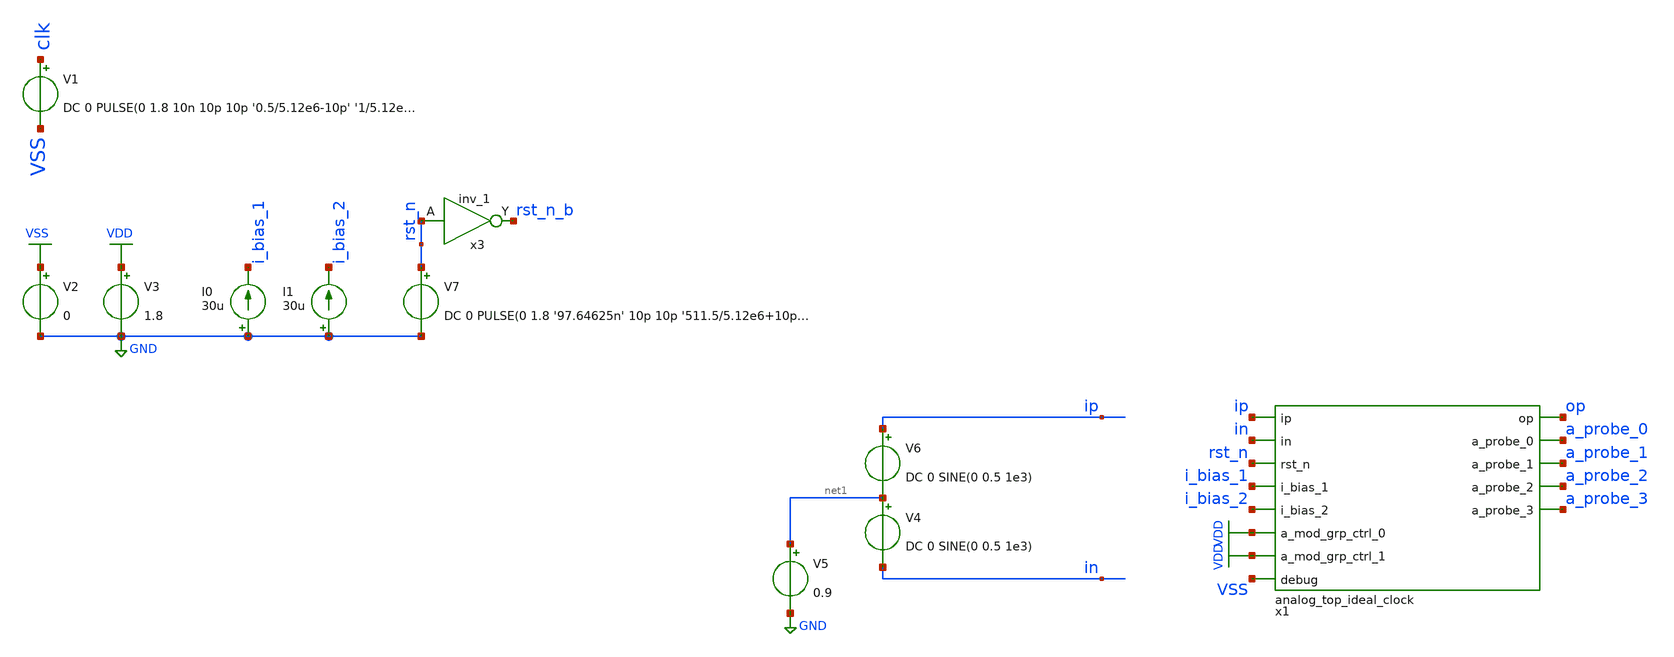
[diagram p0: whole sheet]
** sch_path: verification/schematic_sim/analog_top_ideal_clock_tb.sch
**.subckt analog_top_ideal_clock_tb
V1 clk VSS DC 0 PULSE(0 1.8 10n 10p 10p '0.5/5.12e6-10p' '1/5.12e6')
V2 VSS GND 0
V3 VDD GND 1.8
I0 GND i_bias_1 30u
I1 GND i_bias_2 30u
V5 net1 GND 0.9
V6 ip net1 DC 0 SINE(0 0.5 1e3)
V4 net1 in DC 0 SINE(0 0.5 1e3)
x3 rst_n GND GND VDD VDD rst_n_b sky130_fd_sc_hd__inv_1
V7 rst_n GND DC 0 PULSE(0 1.8 '97.64625n' 10p 10p '511.5/5.12e6+10p' '512/5.12e6')
x1 ip in rst_n i_bias_1 i_bias_2 VDD VDD VSS op a_probe_0 a_probe_1 a_probe_2 a_probe_3 VDD VSS
+ analog_top_ideal_clock
**** begin user architecture code

** opencircuitdesign pdks install
.lib /farmshare/home/classes/ee/372/PDKs/open_pdks_1.0.310/sky130/sky130A/libs.tech/ngspice/sky130.lib.spice tt
.inc /farmshare/home/classes/ee/372/PDKs/open_pdks_1.0.310/sky130/sky130A/libs.ref/sky130_fd_sc_hd/spice/sky130_fd_sc_hd.spice



.control
tran 1u 1m uic
save all
plot v(op)
plot v(x1.op1)
plot v(x1.op2)
*write analog_top_ideal_clock_tb.raw
.endc


**** end user architecture code
**.ends
.GLOBAL GND
.GLOBAL VDD
.GLOBAL VSS
.end
